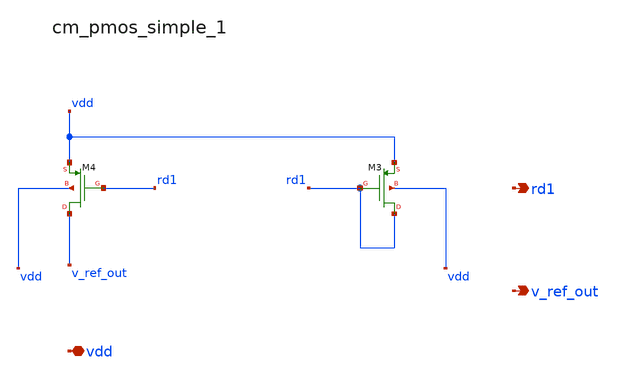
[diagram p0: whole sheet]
** sch_path: analog-db/raw/ldo_005_buffered_ref/hier/blocks/cm_pmos_simple_1.sch
**.subckt cm_pmos_simple_1 vdd rd1 v_ref_out
*.iopin vdd
*.opin rd1
*.opin v_ref_out
XM3 rd1 rd1 vdd vdd sg13_lv_pmos w=x_dut_xm3_w l=x_dut_xm3_l ng=1 m=1
XM4 v_ref_out rd1 vdd vdd sg13_lv_pmos w=x_dut_xm4_w l=x_dut_xm4_l ng=1 m=1
**.ends
.end
